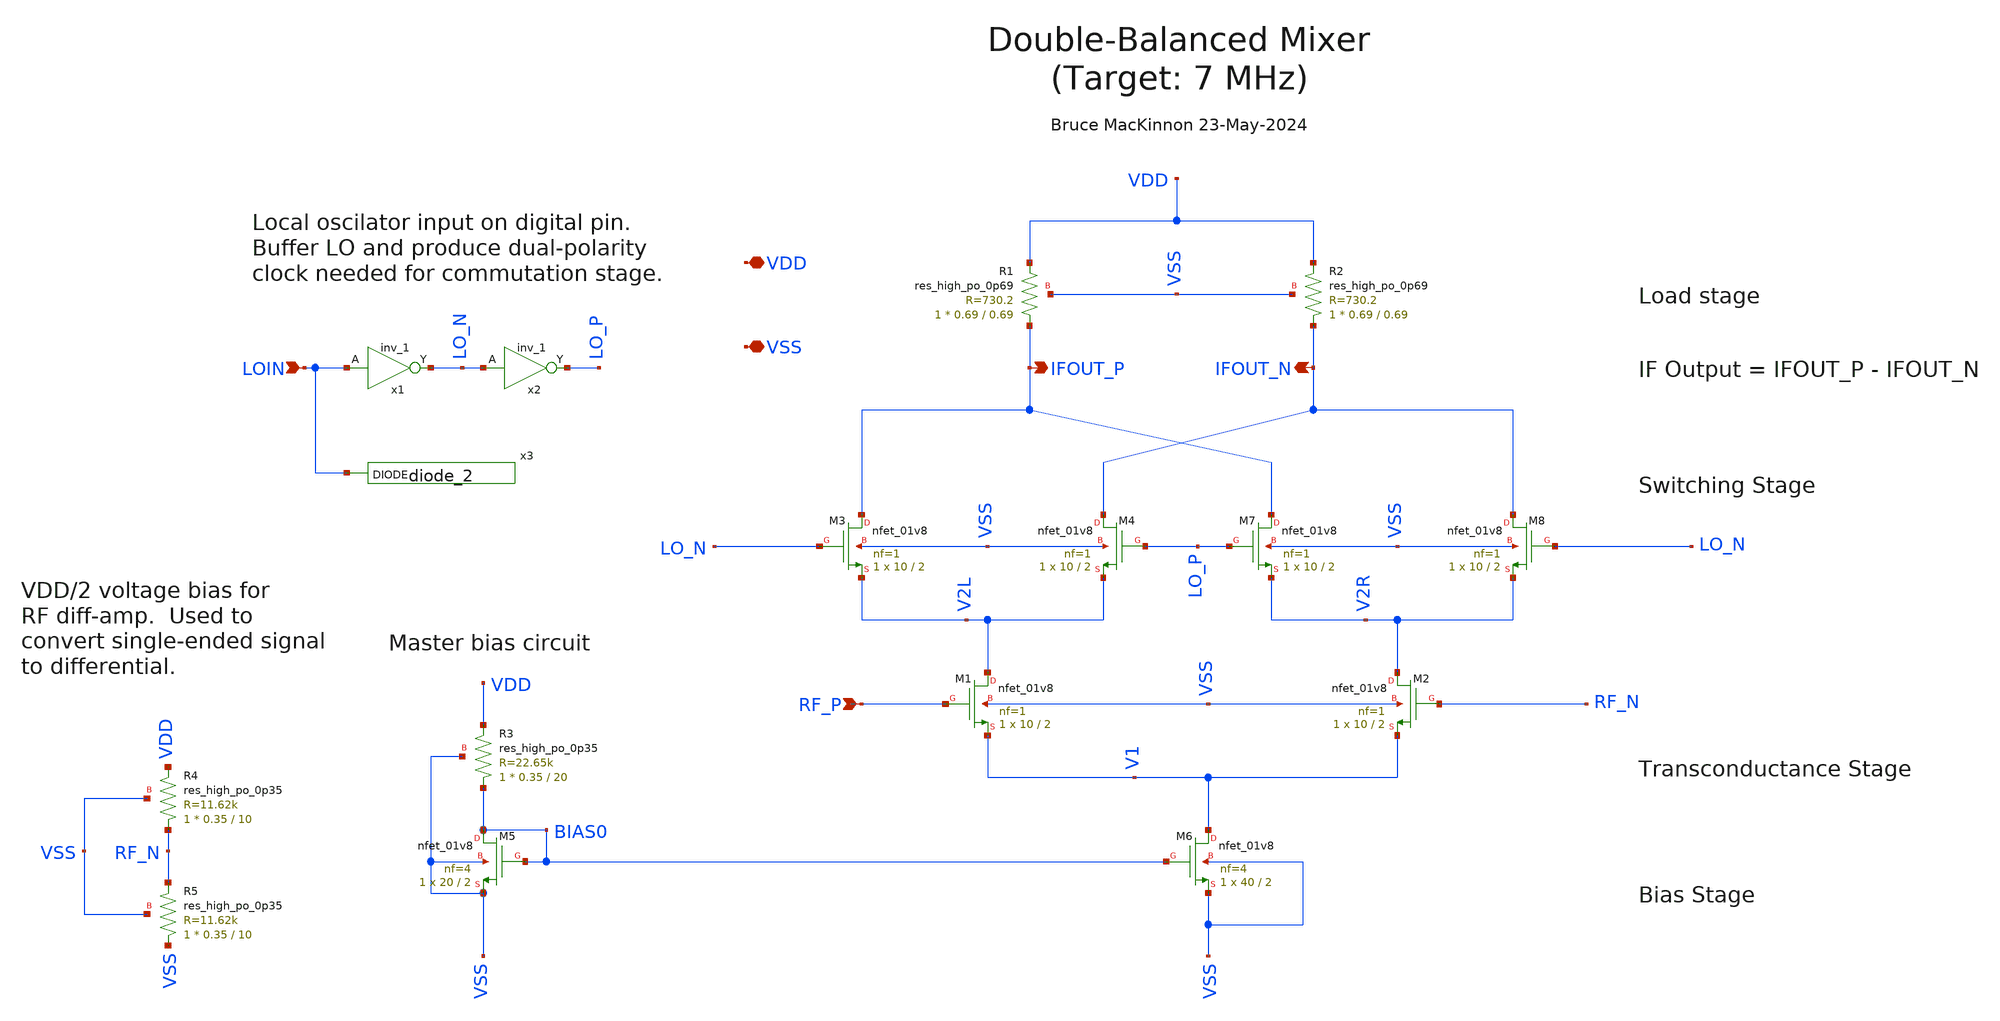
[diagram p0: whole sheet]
** sch_path: xschem/db_mixer.sch
**.subckt db_mixer VDD VSS LOIN IFOUT_P IFOUT_N RF_P
*.iopin VDD
*.iopin VSS
*.ipin LOIN
*.opin IFOUT_P
*.opin IFOUT_N
*.ipin RF_P
XM5 BIAS0 BIAS0 VSS VSS sky130_fd_pr__nfet_01v8 L=2 W=20 nf=4 ad='int((nf+1)/2) * W/nf * 0.29' as='int((nf+2)/2) * W/nf * 0.29'
+ pd='2*int((nf+1)/2) * (W/nf + 0.29)' ps='2*int((nf+2)/2) * (W/nf + 0.29)' nrd='0.29 / W' nrs='0.29 / W'
+ sa=0 sb=0 sd=0 mult=1 m=1
XM6 V1 BIAS0 VSS VSS sky130_fd_pr__nfet_01v8 L=2 W=40 nf=4 ad='int((nf+1)/2) * W/nf * 0.29' as='int((nf+2)/2) * W/nf * 0.29'
+ pd='2*int((nf+1)/2) * (W/nf + 0.29)' ps='2*int((nf+2)/2) * (W/nf + 0.29)' nrd='0.29 / W' nrs='0.29 / W'
+ sa=0 sb=0 sd=0 mult=1 m=1
XR3 BIAS0 VDD VSS sky130_fd_pr__res_high_po_0p35 L=20 mult=1 m=1
x1 LOIN VSS VSS VDD VDD LO_N sky130_fd_sc_hd__inv_1
x2 LO_N VSS VSS VDD VDD LO_P sky130_fd_sc_hd__inv_1
XM1 V2L RF_P V1 VSS sky130_fd_pr__nfet_01v8 L=2 W=10 nf=1 ad='int((nf+1)/2) * W/nf * 0.29' as='int((nf+2)/2) * W/nf * 0.29'
+ pd='2*int((nf+1)/2) * (W/nf + 0.29)' ps='2*int((nf+2)/2) * (W/nf + 0.29)' nrd='0.29 / W' nrs='0.29 / W'
+ sa=0 sb=0 sd=0 mult=1 m=1
XM2 V2R RF_N V1 VSS sky130_fd_pr__nfet_01v8 L=2 W=10 nf=1 ad='int((nf+1)/2) * W/nf * 0.29' as='int((nf+2)/2) * W/nf * 0.29'
+ pd='2*int((nf+1)/2) * (W/nf + 0.29)' ps='2*int((nf+2)/2) * (W/nf + 0.29)' nrd='0.29 / W' nrs='0.29 / W'
+ sa=0 sb=0 sd=0 mult=1 m=1
XM3 IFOUT_P LO_N V2L VSS sky130_fd_pr__nfet_01v8 L=2 W=10 nf=1 ad='int((nf+1)/2) * W/nf * 0.29' as='int((nf+2)/2) * W/nf * 0.29'
+ pd='2*int((nf+1)/2) * (W/nf + 0.29)' ps='2*int((nf+2)/2) * (W/nf + 0.29)' nrd='0.29 / W' nrs='0.29 / W'
+ sa=0 sb=0 sd=0 mult=1 m=1
XM4 IFOUT_N LO_P V2L VSS sky130_fd_pr__nfet_01v8 L=2 W=10 nf=1 ad='int((nf+1)/2) * W/nf * 0.29' as='int((nf+2)/2) * W/nf * 0.29'
+ pd='2*int((nf+1)/2) * (W/nf + 0.29)' ps='2*int((nf+2)/2) * (W/nf + 0.29)' nrd='0.29 / W' nrs='0.29 / W'
+ sa=0 sb=0 sd=0 mult=1 m=1
XM7 IFOUT_P LO_P V2R VSS sky130_fd_pr__nfet_01v8 L=2 W=10 nf=1 ad='int((nf+1)/2) * W/nf * 0.29' as='int((nf+2)/2) * W/nf * 0.29'
+ pd='2*int((nf+1)/2) * (W/nf + 0.29)' ps='2*int((nf+2)/2) * (W/nf + 0.29)' nrd='0.29 / W' nrs='0.29 / W'
+ sa=0 sb=0 sd=0 mult=1 m=1
XM8 IFOUT_N LO_N V2R VSS sky130_fd_pr__nfet_01v8 L=2 W=10 nf=1 ad='int((nf+1)/2) * W/nf * 0.29' as='int((nf+2)/2) * W/nf * 0.29'
+ pd='2*int((nf+1)/2) * (W/nf + 0.29)' ps='2*int((nf+2)/2) * (W/nf + 0.29)' nrd='0.29 / W' nrs='0.29 / W'
+ sa=0 sb=0 sd=0 mult=1 m=1
XR1 IFOUT_P VDD VSS sky130_fd_pr__res_high_po_0p69 L=0.69 mult=1 m=1
XR2 IFOUT_N VDD VSS sky130_fd_pr__res_high_po_0p69 L=0.69 mult=1 m=1
XR4 RF_N VDD VSS sky130_fd_pr__res_high_po_0p35 L=10 mult=1 m=1
XR5 VSS RF_N VSS sky130_fd_pr__res_high_po_0p35 L=10 mult=1 m=1
x3 LOIN VGND VNB VPB VPWR sky130_fd_sc_hd__diode_2
**.ends
.end
